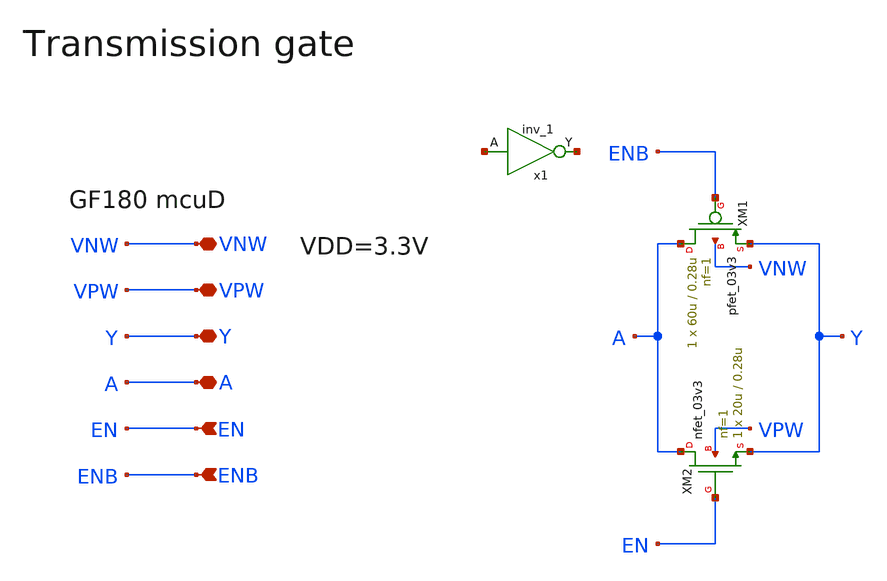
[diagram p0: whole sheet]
** sch_path: designs/libs/core_analog/trans_gate/trans_gate.sch
* Copyright 2022 GlobalFoundries PDK Authors
* Licensed under the Apache License, Version 2.0 (the "License");
* you may not use this file except in compliance with the License.
* You may obtain a copy of the License at
* https://www.apache.org/licenses/LICENSE-2.0
* Unless required by applicable law or agreed to in writing, software
* distributed under the License is distributed on an "AS IS" BASIS,
* WITHOUT WARRANTIES OR CONDITIONS OF ANY KIND, either express or implied.
* See the License for the specific language governing permissions and
* limitations under the License.
**.subckt trans_gate EN ENB VNW VPW Y A
*.ipin EN
*.ipin ENB
*.iopin VNW
*.iopin VPW
*.iopin Y
*.iopin A
XM1 A ENB Y VNW pfet_03v3 L=0.28u W=60u nf=1 ad='int((nf+1)/2) * W/nf * 0.18u' as='int((nf+2)/2) * W/nf * 0.18u'
+ pd='2*int((nf+1)/2) * (W/nf + 0.18u)' ps='2*int((nf+2)/2) * (W/nf + 0.18u)' nrd='0.18u / W' nrs='0.18u / W'
+ sa=0 sb=0 sd=0 m=1
XM2 A EN Y VPW nfet_03v3 L=0.28u W=20u nf=1 ad='int((nf+1)/2) * W/nf * 0.18u' as='int((nf+2)/2) * W/nf * 0.18u'
+ pd='2*int((nf+1)/2) * (W/nf + 0.18u)' ps='2*int((nf+2)/2) * (W/nf + 0.18u)' nrd='0.18u / W' nrs='0.18u / W'
+ sa=0 sb=0 sd=0 m=1
x1 net1 net2 VDD VDD GND GND gf180mcu_fd_sc_mcu7t5v0__inv_1
**.ends
.end
